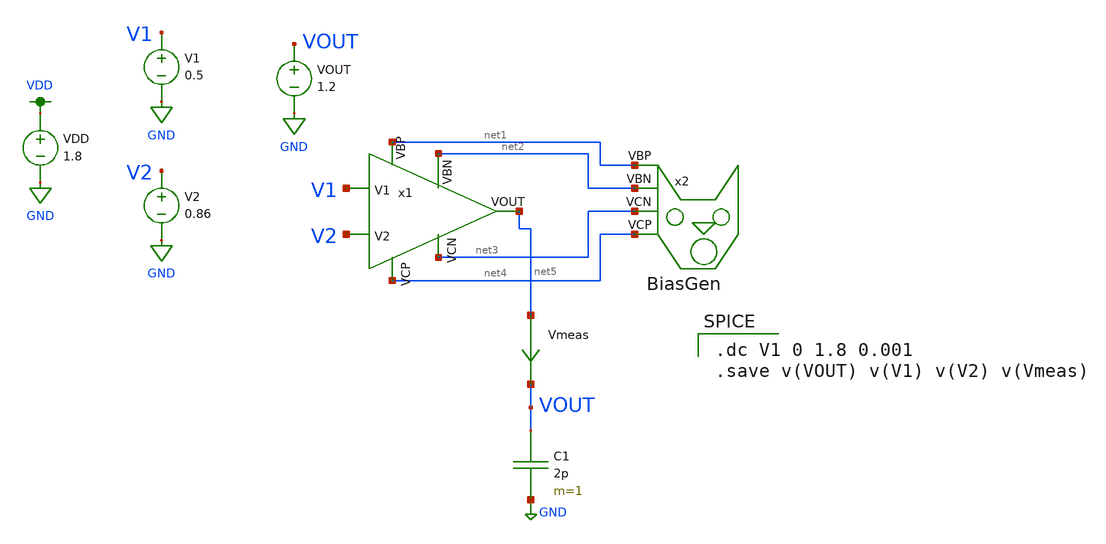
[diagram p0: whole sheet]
** sch_path: MP3/test_harness.sch
**.subckt test_harness
x1 net1 net4 V2 net5 V1 net3 net2 FCDA
x2 net1 net4 net3 net2 BiasGen
V1 V1 GND 0.5
V2 V2 GND 0.86
VDD VDD GND 1.8
C1 VOUT GND 2p m=1
VOUT VOUT GND 1.2
Vmeas net5 VOUT 0
.save i(vmeas)
**** begin user architecture code

.option wnflag=1
.lib ~/skywater/skywater-pdk/libraries/sky130_fd_pr_ngspice/latest/models/sky130.lib.spice tt


.dc V1 0 1.8 0.001
.save v(VOUT) v(V1) v(V2) v(Vmeas)

**** end user architecture code
**.ends

* expanding   symbol:  /home/madvlsi/Documents/MP3/FCDA.sym # of pins=7
** sym_path: MP3/FCDA.sym
** sch_path: MP3/FCDA.sch
.subckt FCDA VBP VCP V2 VOUT V1 VCN VBN
*.ipin V2
*.ipin V1
*.ipin VBN
*.ipin VCN
*.ipin VCP
*.ipin VBP
*.opin VOUT
XM1 net2 V1 net1 GND sky130_fd_pr__nfet_01v8 L=0.5 W=12 nf=1 ad='int((nf+1)/2) * W/nf * 0.29' as='int((nf+2)/2) * W/nf * 0.29'
+ pd='2*int((nf+1)/2) * (W/nf + 0.29)' ps='2*int((nf+2)/2) * (W/nf + 0.29)' nrd='0.29 / W' nrs='0.29 / W'
+ sa=0 sb=0 sd=0 mult=1 m=1
XM2 net3 V2 net1 GND sky130_fd_pr__nfet_01v8 L=0.5 W=12 nf=1 ad='int((nf+1)/2) * W/nf * 0.29' as='int((nf+2)/2) * W/nf * 0.29'
+ pd='2*int((nf+1)/2) * (W/nf + 0.29)' ps='2*int((nf+2)/2) * (W/nf + 0.29)' nrd='0.29 / W' nrs='0.29 / W'
+ sa=0 sb=0 sd=0 mult=1 m=1
XM3 net2 VBP VDD VDD sky130_fd_pr__pfet_01v8 L=0.5 W=12 nf=1 ad='int((nf+1)/2) * W/nf * 0.29' as='int((nf+2)/2) * W/nf * 0.29'
+ pd='2*int((nf+1)/2) * (W/nf + 0.29)' ps='2*int((nf+2)/2) * (W/nf + 0.29)' nrd='0.29 / W' nrs='0.29 / W'
+ sa=0 sb=0 sd=0 mult=1 m=1
XM4 net3 VBP VDD VDD sky130_fd_pr__pfet_01v8 L=0.5 W=12 nf=1 ad='int((nf+1)/2) * W/nf * 0.29' as='int((nf+2)/2) * W/nf * 0.29'
+ pd='2*int((nf+1)/2) * (W/nf + 0.29)' ps='2*int((nf+2)/2) * (W/nf + 0.29)' nrd='0.29 / W' nrs='0.29 / W'
+ sa=0 sb=0 sd=0 mult=1 m=1
XM5 net4 VCP net2 VDD sky130_fd_pr__pfet_01v8 L=0.5 W=12 nf=1 ad='int((nf+1)/2) * W/nf * 0.29' as='int((nf+2)/2) * W/nf * 0.29'
+ pd='2*int((nf+1)/2) * (W/nf + 0.29)' ps='2*int((nf+2)/2) * (W/nf + 0.29)' nrd='0.29 / W' nrs='0.29 / W'
+ sa=0 sb=0 sd=0 mult=1 m=1
XM6 VOUT VCP net3 VDD sky130_fd_pr__pfet_01v8 L=0.5 W=12 nf=1 ad='int((nf+1)/2) * W/nf * 0.29' as='int((nf+2)/2) * W/nf * 0.29'
+ pd='2*int((nf+1)/2) * (W/nf + 0.29)' ps='2*int((nf+2)/2) * (W/nf + 0.29)' nrd='0.29 / W' nrs='0.29 / W'
+ sa=0 sb=0 sd=0 mult=1 m=1
XM7 net5 net4 GND GND sky130_fd_pr__nfet_01v8 L=0.5 W=12 nf=1 ad='int((nf+1)/2) * W/nf * 0.29' as='int((nf+2)/2) * W/nf * 0.29'
+ pd='2*int((nf+1)/2) * (W/nf + 0.29)' ps='2*int((nf+2)/2) * (W/nf + 0.29)' nrd='0.29 / W' nrs='0.29 / W'
+ sa=0 sb=0 sd=0 mult=1 m=1
XM8 net6 net4 GND GND sky130_fd_pr__nfet_01v8 L=0.5 W=12 nf=1 ad='int((nf+1)/2) * W/nf * 0.29' as='int((nf+2)/2) * W/nf * 0.29'
+ pd='2*int((nf+1)/2) * (W/nf + 0.29)' ps='2*int((nf+2)/2) * (W/nf + 0.29)' nrd='0.29 / W' nrs='0.29 / W'
+ sa=0 sb=0 sd=0 mult=1 m=1
XM9 net4 VCN net5 GND sky130_fd_pr__nfet_01v8 L=0.5 W=12 nf=1 ad='int((nf+1)/2) * W/nf * 0.29' as='int((nf+2)/2) * W/nf * 0.29'
+ pd='2*int((nf+1)/2) * (W/nf + 0.29)' ps='2*int((nf+2)/2) * (W/nf + 0.29)' nrd='0.29 / W' nrs='0.29 / W'
+ sa=0 sb=0 sd=0 mult=1 m=1
XM10 VOUT VCN net6 GND sky130_fd_pr__nfet_01v8 L=0.5 W=12 nf=1 ad='int((nf+1)/2) * W/nf * 0.29' as='int((nf+2)/2) * W/nf * 0.29'
+ pd='2*int((nf+1)/2) * (W/nf + 0.29)' ps='2*int((nf+2)/2) * (W/nf + 0.29)' nrd='0.29 / W' nrs='0.29 / W'
+ sa=0 sb=0 sd=0 mult=1 m=1
XMb net1 VBN GND GND sky130_fd_pr__nfet_01v8 L=0.5 W=12 nf=1 ad='int((nf+1)/2) * W/nf * 0.29' as='int((nf+2)/2) * W/nf * 0.29'
+ pd='2*int((nf+1)/2) * (W/nf + 0.29)' ps='2*int((nf+2)/2) * (W/nf + 0.29)' nrd='0.29 / W' nrs='0.29 / W'
+ sa=0 sb=0 sd=0 mult=1 m=1
.ends


* expanding   symbol:  /home/madvlsi/Documents/MP3/BiasGen.sym # of pins=4
** sym_path: MP3/BiasGen.sym
** sch_path: MP3/BiasGen.sch
.subckt BiasGen VBP VCP VCN VBN
*.opin VCN
*.opin VCP
*.opin VBP
*.opin VBN
XM1 net1 net1 net2 GND sky130_fd_pr__nfet_01v8 L=0.5 W=48 nf=1 ad='int((nf+1)/2) * W/nf * 0.29' as='int((nf+2)/2) * W/nf * 0.29'
+ pd='2*int((nf+1)/2) * (W/nf + 0.29)' ps='2*int((nf+2)/2) * (W/nf + 0.29)' nrd='0.29 / W' nrs='0.29 / W'
+ sa=0 sb=0 sd=0 mult=1 m=1
XM2 net2 net1 GND GND sky130_fd_pr__nfet_01v8 L=0.5 W=12 nf=1 ad='int((nf+1)/2) * W/nf * 0.29' as='int((nf+2)/2) * W/nf * 0.29'
+ pd='2*int((nf+1)/2) * (W/nf + 0.29)' ps='2*int((nf+2)/2) * (W/nf + 0.29)' nrd='0.29 / W' nrs='0.29 / W'
+ sa=0 sb=0 sd=0 mult=1 m=1
XM3 VCN VCN net2 GND sky130_fd_pr__nfet_01v8 L=0.5 W=12 nf=1 ad='int((nf+1)/2) * W/nf * 0.29' as='int((nf+2)/2) * W/nf * 0.29'
+ pd='2*int((nf+1)/2) * (W/nf + 0.29)' ps='2*int((nf+2)/2) * (W/nf + 0.29)' nrd='0.29 / W' nrs='0.29 / W'
+ sa=0 sb=0 sd=0 mult=1 m=1
XM4 net1 VBP VDD VDD sky130_fd_pr__pfet_01v8 L=2.5 W=12 nf=1 ad='int((nf+1)/2) * W/nf * 0.29' as='int((nf+2)/2) * W/nf * 0.29'
+ pd='2*int((nf+1)/2) * (W/nf + 0.29)' ps='2*int((nf+2)/2) * (W/nf + 0.29)' nrd='0.29 / W' nrs='0.29 / W'
+ sa=0 sb=0 sd=0 mult=1 m=1
XM5 VCN VBP VDD VDD sky130_fd_pr__pfet_01v8 L=0.5 W=12 nf=1 ad='int((nf+1)/2) * W/nf * 0.29' as='int((nf+2)/2) * W/nf * 0.29'
+ pd='2*int((nf+1)/2) * (W/nf + 0.29)' ps='2*int((nf+2)/2) * (W/nf + 0.29)' nrd='0.29 / W' nrs='0.29 / W'
+ sa=0 sb=0 sd=0 mult=1 m=1
XM6 net4 net3 VDD VDD sky130_fd_pr__pfet_01v8 L=0.5 W=12 nf=1 ad='int((nf+1)/2) * W/nf * 0.29' as='int((nf+2)/2) * W/nf * 0.29'
+ pd='2*int((nf+1)/2) * (W/nf + 0.29)' ps='2*int((nf+2)/2) * (W/nf + 0.29)' nrd='0.29 / W' nrs='0.29 / W'
+ sa=0 sb=0 sd=0 mult=1 m=1
XM7 net3 net3 net4 VDD sky130_fd_pr__pfet_01v8 L=0.5 W=48 nf=1 ad='int((nf+1)/2) * W/nf * 0.29' as='int((nf+2)/2) * W/nf * 0.29'
+ pd='2*int((nf+1)/2) * (W/nf + 0.29)' ps='2*int((nf+2)/2) * (W/nf + 0.29)' nrd='0.29 / W' nrs='0.29 / W'
+ sa=0 sb=0 sd=0 mult=1 m=1
XM8 VCP VCP net4 VDD sky130_fd_pr__pfet_01v8 L=0.5 W=12 nf=1 ad='int((nf+1)/2) * W/nf * 0.29' as='int((nf+2)/2) * W/nf * 0.29'
+ pd='2*int((nf+1)/2) * (W/nf + 0.29)' ps='2*int((nf+2)/2) * (W/nf + 0.29)' nrd='0.29 / W' nrs='0.29 / W'
+ sa=0 sb=0 sd=0 mult=1 m=1
XM9 net3 VBN GND GND sky130_fd_pr__nfet_01v8 L=2.5 W=12 nf=1 ad='int((nf+1)/2) * W/nf * 0.29' as='int((nf+2)/2) * W/nf * 0.29'
+ pd='2*int((nf+1)/2) * (W/nf + 0.29)' ps='2*int((nf+2)/2) * (W/nf + 0.29)' nrd='0.29 / W' nrs='0.29 / W'
+ sa=0 sb=0 sd=0 mult=1 m=1
XM10 VCP VBN GND GND sky130_fd_pr__nfet_01v8 L=0.5 W=12 nf=1 ad='int((nf+1)/2) * W/nf * 0.29' as='int((nf+2)/2) * W/nf * 0.29'
+ pd='2*int((nf+1)/2) * (W/nf + 0.29)' ps='2*int((nf+2)/2) * (W/nf + 0.29)' nrd='0.29 / W' nrs='0.29 / W'
+ sa=0 sb=0 sd=0 mult=1 m=1
XM11 VBP VBP VDD VDD sky130_fd_pr__pfet_01v8 L=0.5 W=12 nf=1 ad='int((nf+1)/2) * W/nf * 0.29' as='int((nf+2)/2) * W/nf * 0.29'
+ pd='2*int((nf+1)/2) * (W/nf + 0.29)' ps='2*int((nf+2)/2) * (W/nf + 0.29)' nrd='0.29 / W' nrs='0.29 / W'
+ sa=0 sb=0 sd=0 mult=1 m=1
XM12 VBP VBN GND GND sky130_fd_pr__nfet_01v8 L=0.5 W=12 nf=1 ad='int((nf+1)/2) * W/nf * 0.29' as='int((nf+2)/2) * W/nf * 0.29'
+ pd='2*int((nf+1)/2) * (W/nf + 0.29)' ps='2*int((nf+2)/2) * (W/nf + 0.29)' nrd='0.29 / W' nrs='0.29 / W'
+ sa=0 sb=0 sd=0 mult=1 m=1
XM13 VBN VBN GND GND sky130_fd_pr__nfet_01v8 L=0.5 W=12 nf=1 ad='int((nf+1)/2) * W/nf * 0.29' as='int((nf+2)/2) * W/nf * 0.29'
+ pd='2*int((nf+1)/2) * (W/nf + 0.29)' ps='2*int((nf+2)/2) * (W/nf + 0.29)' nrd='0.29 / W' nrs='0.29 / W'
+ sa=0 sb=0 sd=0 mult=1 m=1
IB GND VBN 1u
.ends

.GLOBAL GND
.GLOBAL VDD
.end
